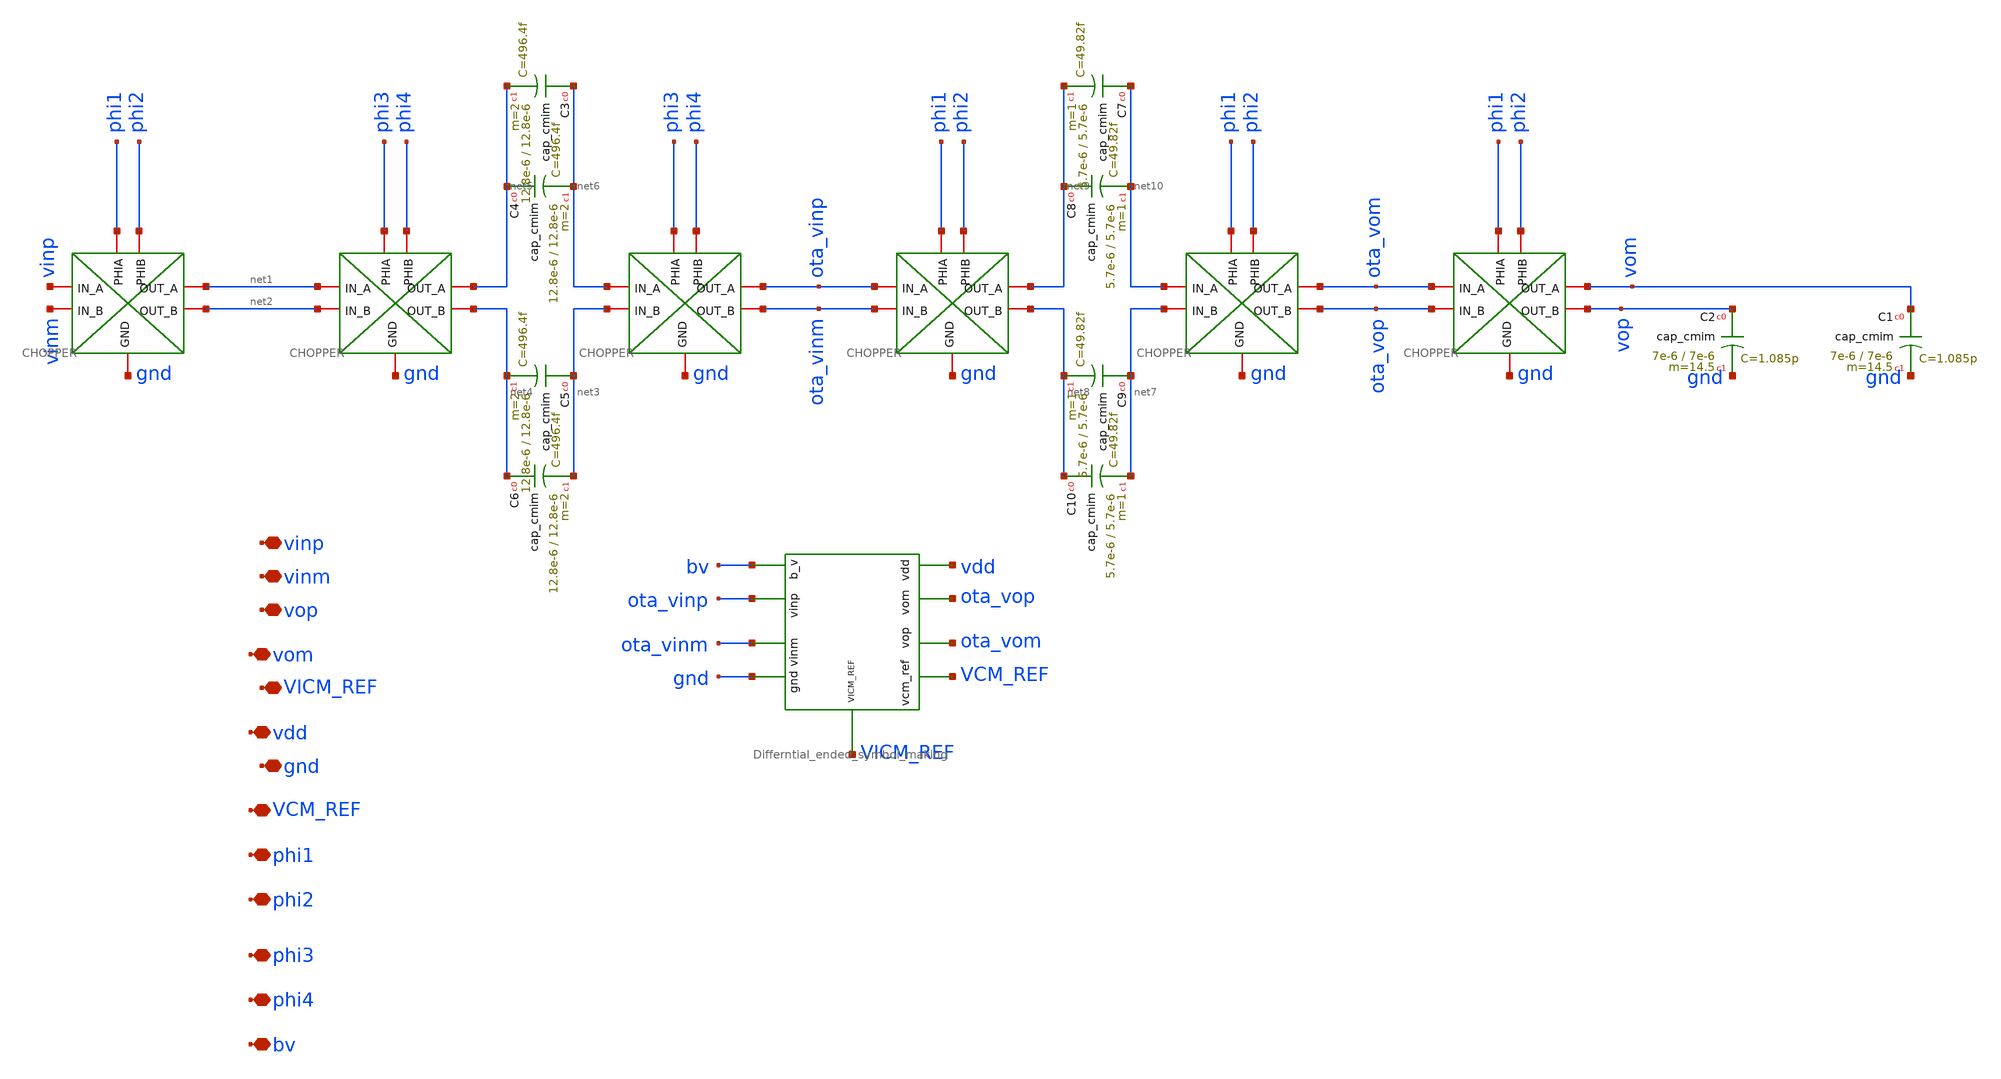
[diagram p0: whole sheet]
** sch_path: imp_boost_tech.sch
**.subckt imp_boost_tech vinp vinm vop vom phi1 phi2 phi3 phi4 VICM_REF bv gnd vdd VCM_REF
*.iopin vinp
*.iopin vinm
*.iopin vop
*.iopin vom
*.iopin phi1
*.iopin phi2
*.iopin phi3
*.iopin phi4
*.iopin VICM_REF
*.iopin bv
*.iopin gnd
*.iopin vdd
*.iopin VCM_REF
XC3 net6 net5 cap_cmim w=12.8e-6 l=12.8e-6 m=2 mm_ok=1
XC4 net5 net6 cap_cmim w=12.8e-6 l=12.8e-6 m=2 mm_ok=1
XC5 net3 net4 cap_cmim w=12.8e-6 l=12.8e-6 m=2 mm_ok=1
XC6 net4 net3 cap_cmim w=12.8e-6 l=12.8e-6 m=2 mm_ok=1
XC7 net10 net9 cap_cmim w=5.7e-6 l=5.7e-6 m=1 mm_ok=1
XC8 net9 net10 cap_cmim w=5.7e-6 l=5.7e-6 m=1 mm_ok=1
XC9 net7 net8 cap_cmim w=5.7e-6 l=5.7e-6 m=1 mm_ok=1
XC10 net8 net7 cap_cmim w=5.7e-6 l=5.7e-6 m=1 mm_ok=1
XC1 vom gnd cap_cmim w=7e-6 l=7e-6 m=14.5 mm_ok=1
XC2 vop gnd cap_cmim w=7e-6 l=7e-6 m=14.5 mm_ok=1
x8 phi1 net1 vinp phi2 net2 vinm gnd CHOPPER
x1 phi3 net5 net1 phi4 net4 net2 gnd CHOPPER
x3 phi3 ota_vinp net6 phi4 ota_vinm net3 gnd CHOPPER
x4 phi1 net9 ota_vinp phi2 net8 ota_vinm gnd CHOPPER
x5 phi1 ota_vom net10 phi2 ota_vop net7 gnd CHOPPER
x6 phi1 vom ota_vom phi2 vop ota_vop gnd CHOPPER
x7 vdd VCM_REF ota_vop ota_vom gnd bv ota_vinm ota_vinp VICM_REF Differntial_ended_symbol_making
**.ends
.end
